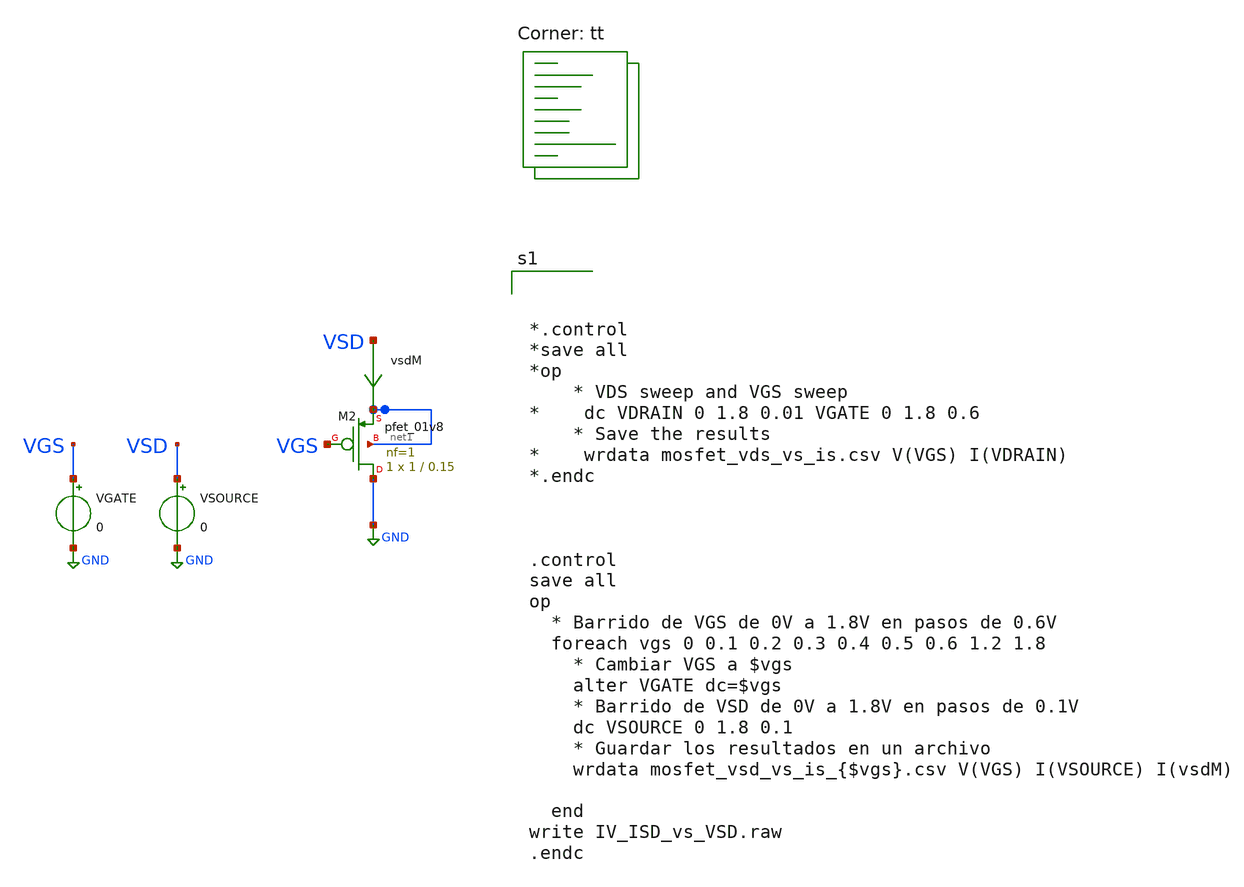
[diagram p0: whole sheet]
** sch_path: circuits/copys_to_develop_pmos/IV_ISD_vs_VSD?.sch
**.subckt IV_ISD_vs_VSD?
VGATE VGS GND 0
VSOURCE VSD GND 0
vsdM VSD net1 0
.save i(vsdm)
XM2 GND VGS net1 net1 sky130_fd_pr__pfet_01v8 L=0.15 W=1 nf=1 ad='int((nf+1)/2) * W/nf * 0.29' as='int((nf+2)/2) * W/nf * 0.29'
+ pd='2*int((nf+1)/2) * (W/nf + 0.29)' ps='2*int((nf+2)/2) * (W/nf + 0.29)' nrd='0.29 / W' nrs='0.29 / W'
+ sa=0 sb=0 sd=0 mult=1 m=1
**** begin user architecture code



*.control
*save all
*op
    * VDS sweep and VGS sweep
*    dc VDRAIN 0 1.8 0.01 VGATE 0 1.8 0.6
    * Save the results
*    wrdata mosfet_vds_vs_is.csv V(VGS) I(VDRAIN)
*.endc



.control
save all
op
  * Barrido de VGS de 0V a 1.8V en pasos de 0.6V
  foreach vgs 0 0.1 0.2 0.3 0.4 0.5 0.6 1.2 1.8
    * Cambiar VGS a $vgs
    alter VGATE dc=$vgs
    * Barrido de VSD de 0V a 1.8V en pasos de 0.1V
    dc VSOURCE 0 1.8 0.1
    * Guardar los resultados en un archivo
    wrdata mosfet_vsd_vs_is_{$vgs}.csv V(VGS) I(VSOURCE) I(vsdM)

  end
write IV_ISD_vs_VSD.raw
.endc



.lib $::SKYWATER_MODELS/sky130.lib.spice tt
**** end user architecture code
**.ends
.GLOBAL GND
.end
